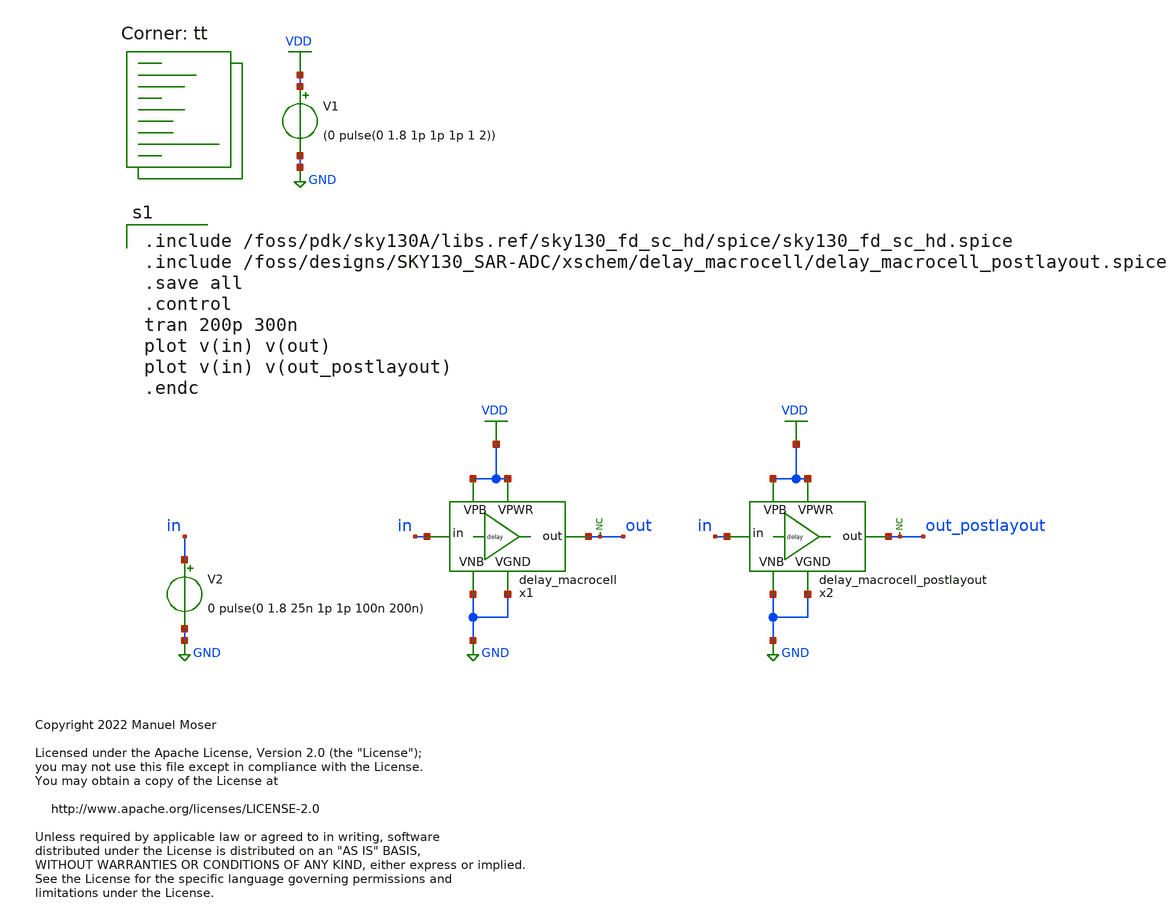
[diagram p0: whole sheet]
** sch_path: xschem/delay_macrocell/delay_macrocell_tb.sch
* Copyright 2022 Manuel Moser
* Licensed under the Apache License, Version 2.0 (the "License");
**.subckt delay_macrocell_tb
V1 VDD GND (0 pulse(0 1.8 1p 1p 1p 1 2))
V2 in GND 0 pulse(0 1.8 25n 1p 1p 100n 200n)
x1 VDD in out GND GND VDD delay_macrocell
* noconn out
* noconn out_postlayout
x2 VDD in out_postlayout GND GND VDD delay_macrocell_postlayout
**** begin user architecture code

.include /foss/pdk/sky130A/libs.ref/sky130_fd_sc_hd/spice/sky130_fd_sc_hd.spice
.include /foss/designs/SKY130_SAR-ADC/xschem/delay_macrocell/delay_macrocell_postlayout.spice
.save all
.control
tran 200p 300n
plot v(in) v(out)
plot v(in) v(out_postlayout)
.endc

.lib $::SKYWATER_MODELS/sky130.lib.spice tt
**** end user architecture code
**.ends

* expanding   symbol:  delay_macrocell.sym # of pins=6
** sym_path: xschem/delay_macrocell/delay_macrocell.sym
** sch_path: xschem/delay_macrocell/delay_macrocell.sch
.subckt delay_macrocell VPWR in out VGND VNB VPB
*.iopin VPWR
*.iopin VGND
*.ipin in
*.opin out
*.iopin VPB
*.iopin VNB
XM2 net1 in VGND VNB sky130_fd_pr__nfet_01v8 L=4 W=0.42 nf=1 ad='int((nf+1)/2) * W/nf * 0.29' as='int((nf+2)/2) * W/nf * 0.29'
+ pd='2*int((nf+1)/2) * (W/nf + 0.29)' ps='2*int((nf+2)/2) * (W/nf + 0.29)' nrd='0.29 / W' nrs='0.29 / W'
+ sa=0 sb=0 sd=0 mult=1 m=1
XM3 net3 net1 VGND VNB sky130_fd_pr__nfet_01v8 L=0.15 W=0.84 nf=2 ad='int((nf+1)/2) * W/nf * 0.29' as='int((nf+2)/2) * W/nf * 0.29'
+ pd='2*int((nf+1)/2) * (W/nf + 0.29)' ps='2*int((nf+2)/2) * (W/nf + 0.29)' nrd='0.29 / W' nrs='0.29 / W'
+ sa=0 sb=0 sd=0 mult=1 m=1
XM4 out net1 net3 VNB sky130_fd_pr__nfet_01v8 L=0.15 W=0.84 nf=2 ad='int((nf+1)/2) * W/nf * 0.29' as='int((nf+2)/2) * W/nf * 0.29'
+ pd='2*int((nf+1)/2) * (W/nf + 0.29)' ps='2*int((nf+2)/2) * (W/nf + 0.29)' nrd='0.29 / W' nrs='0.29 / W'
+ sa=0 sb=0 sd=0 mult=1 m=1
XM5 out net1 net2 VPB sky130_fd_pr__pfet_01v8 L=0.15 W=1.6 nf=2 ad='int((nf+1)/2) * W/nf * 0.29' as='int((nf+2)/2) * W/nf * 0.29'
+ pd='2*int((nf+1)/2) * (W/nf + 0.29)' ps='2*int((nf+2)/2) * (W/nf + 0.29)' nrd='0.29 / W' nrs='0.29 / W'
+ sa=0 sb=0 sd=0 mult=1 m=1
XM6 net2 net1 VPWR VPB sky130_fd_pr__pfet_01v8 L=0.15 W=1.6 nf=2 ad='int((nf+1)/2) * W/nf * 0.29' as='int((nf+2)/2) * W/nf * 0.29'
+ pd='2*int((nf+1)/2) * (W/nf + 0.29)' ps='2*int((nf+2)/2) * (W/nf + 0.29)' nrd='0.29 / W' nrs='0.29 / W'
+ sa=0 sb=0 sd=0 mult=1 m=1
XM7 VPWR out net3 VNB sky130_fd_pr__nfet_01v8 L=0.15 W=0.42 nf=1 ad='int((nf+1)/2) * W/nf * 0.29' as='int((nf+2)/2) * W/nf * 0.29'
+ pd='2*int((nf+1)/2) * (W/nf + 0.29)' ps='2*int((nf+2)/2) * (W/nf + 0.29)' nrd='0.29 / W' nrs='0.29 / W'
+ sa=0 sb=0 sd=0 mult=1 m=1
XM8 VGND out net2 VPB sky130_fd_pr__pfet_01v8 L=0.15 W=0.8 nf=1 ad='int((nf+1)/2) * W/nf * 0.29' as='int((nf+2)/2) * W/nf * 0.29'
+ pd='2*int((nf+1)/2) * (W/nf + 0.29)' ps='2*int((nf+2)/2) * (W/nf + 0.29)' nrd='0.29 / W' nrs='0.29 / W'
+ sa=0 sb=0 sd=0 mult=1 m=1
XM1 net1 in VPWR VPB sky130_fd_pr__pfet_01v8 L=4 W=0.8 nf=1 ad='int((nf+1)/2) * W/nf * 0.29' as='int((nf+2)/2) * W/nf * 0.29'
+ pd='2*int((nf+1)/2) * (W/nf + 0.29)' ps='2*int((nf+2)/2) * (W/nf + 0.29)' nrd='0.29 / W' nrs='0.29 / W'
+ sa=0 sb=0 sd=0 mult=1 m=1
XC1 net1 VGND sky130_fd_pr__cap_mim_m3_1 W=3.68 L=1.93 MF=1 m=1
XC2 net1 VGND sky130_fd_pr__cap_mim_m3_1 W=3.26 L=1.93 MF=1 m=1
.ends

.GLOBAL VDD
.GLOBAL GND
.end
